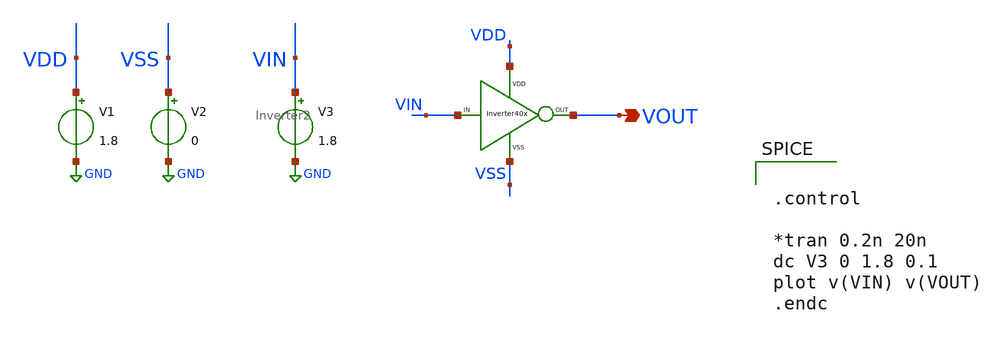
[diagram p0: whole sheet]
** sch_path: xschem/DC_DC_Converter_xschem/OTHERS/DC_DC_Converter_JV10/Inverter_2/Inverter2_TB.sch
**.subckt Inverter2_TB VOUT
*.opin VOUT
V1 VDD GND 1.8
V2 VSS GND 0
V3 VIN GND 1.8
X1 VIN VOUT VDD VSS Inverter2
**** begin user architecture code


.control

*tran 0.2n 20n
dc V3 0 1.8 0.1
plot v(VIN) v(VOUT)
.endc



** opencircuitdesign pdks install
.lib $::SKYWATER_MODELS/sky130.lib.spice tt


**** end user architecture code
**.ends
.GLOBAL GND
.end
